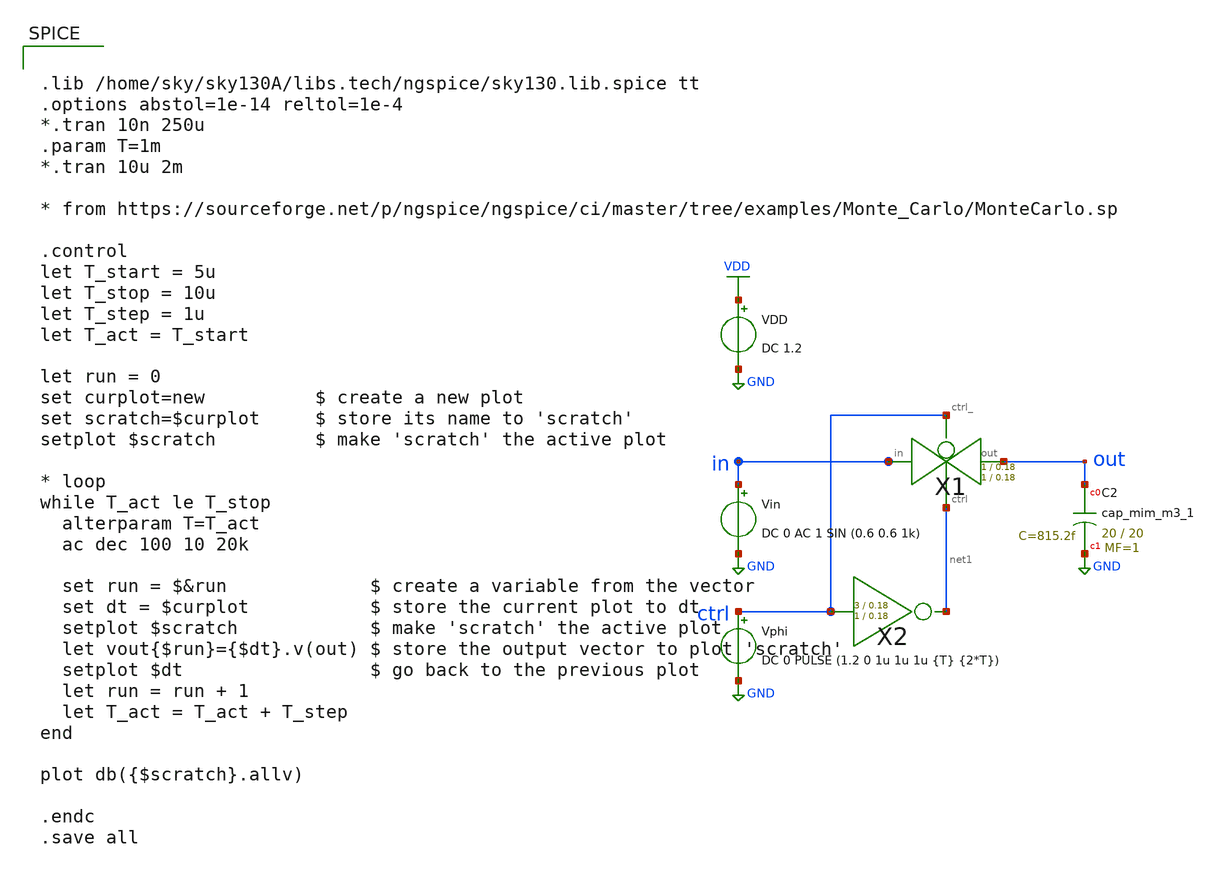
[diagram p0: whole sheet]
** sch_path: xschem/Switched_Caps/Characterizer_tranmission_gate_plot_sweep.sch
**.subckt Characterizer_tranmission_gate_plot_sweep
Vphi ctrl GND DC 0 PULSE (1.2 0 1u 1u 1u {T} {2*T})
XC2 out GND sky130_fd_pr__cap_mim_m3_1 W=20 L=20 MF=1 m=1
Vin in GND DC 0 AC 1 SIN (0.6 0.6 1k)
X1 in out ctrl net1 transmission_gate Wpmos=1 Lpmos=0.18 Wnmos=1 Lnmos=0.18
X2 ctrl net1 inv Wpmos=3 Lpmos=0.18 Wnmos=1 Lnmos=0.18
VDD VDD GND DC 1.2
**** begin user architecture code


.lib /home/sky/sky130A/libs.tech/ngspice/sky130.lib.spice tt
.options abstol=1e-14 reltol=1e-4
*.tran 10n 250u
.param T=1m
*.tran 10u 2m

* from https://sourceforge.net/p/ngspice/ngspice/ci/master/tree/examples/Monte_Carlo/MonteCarlo.sp

.control
let T_start = 5u
let T_stop = 10u
let T_step = 1u
let T_act = T_start

let run = 0
set curplot=new          $ create a new plot
set scratch=$curplot     $ store its name to 'scratch'
setplot $scratch         $ make 'scratch' the active plot

* loop
while T_act le T_stop
  alterparam T=T_act
  ac dec 100 10 20k

  set run = $&run             $ create a variable from the vector
  set dt = $curplot           $ store the current plot to dt
  setplot $scratch            $ make 'scratch' the active plot
  let vout{$run}={$dt}.v(out) $ store the output vector to plot 'scratch'
  setplot $dt                 $ go back to the previous plot
  let run = run + 1
  let T_act = T_act + T_step
end

plot db({$scratch}.allv)

.endc
.save all


**** end user architecture code
**.ends

* expanding   symbol:  transmission_gate/transmission_gate.sym # of pins=4
** sym_path: xschem/transmission_gate/transmission_gate.sym
** sch_path: xschem/transmission_gate/transmission_gate.sch
.subckt transmission_gate in out ctrl_ ctrl  Wpmos=1 Lpmos=0.18 Wnmos=1 Lnmos=0.18
*.iopin in
*.iopin out
*.ipin ctrl_
*.ipin ctrl
XM1 in ctrl out GND sky130_fd_pr__nfet_01v8 L=Lnmos W=Wnmos nf=1 ad='int((nf+1)/2) * W/nf * 0.29' as='int((nf+2)/2) * W/nf * 0.29'
+ pd='2*int((nf+1)/2) * (W/nf + 0.29)' ps='2*int((nf+2)/2) * (W/nf + 0.29)' nrd='0.29 / W' nrs='0.29 / W'
+ sa=0 sb=0 sd=0 mult=1 m=1
XM2 out ctrl_ in VDD sky130_fd_pr__pfet_01v8 L=Lpmos W=Wpmos nf=1 ad='int((nf+1)/2) * W/nf * 0.29' as='int((nf+2)/2) * W/nf * 0.29'
+ pd='2*int((nf+1)/2) * (W/nf + 0.29)' ps='2*int((nf+2)/2) * (W/nf + 0.29)' nrd='0.29 / W' nrs='0.29 / W'
+ sa=0 sb=0 sd=0 mult=1 m=1
.ends


* expanding   symbol:  inv/inv.sym # of pins=2
** sym_path: xschem/inv/inv.sym
** sch_path: xschem/inv/inv.sch
.subckt inv in out  Wpmos=3 Lpmos=0.18 Wnmos=1 Lnmos=0.18
*.ipin in
*.iopin out
XM1 out in GND GND sky130_fd_pr__nfet_01v8 L=Lnmos W=Wnmos nf=1 ad='int((nf+1)/2) * W/nf * 0.29' as='int((nf+2)/2) * W/nf * 0.29'
+ pd='2*int((nf+1)/2) * (W/nf + 0.29)' ps='2*int((nf+2)/2) * (W/nf + 0.29)' nrd='0.29 / W' nrs='0.29 / W'
+ sa=0 sb=0 sd=0 mult=1 m=1
XM2 out in VDD VDD sky130_fd_pr__pfet_01v8 L=Lpmos W=Wpmos nf=1 ad='int((nf+1)/2) * W/nf * 0.29' as='int((nf+2)/2) * W/nf * 0.29'
+ pd='2*int((nf+1)/2) * (W/nf + 0.29)' ps='2*int((nf+2)/2) * (W/nf + 0.29)' nrd='0.29 / W' nrs='0.29 / W'
+ sa=0 sb=0 sd=0 mult=1 m=1
.ends

.GLOBAL GND
.GLOBAL VDD
.end
